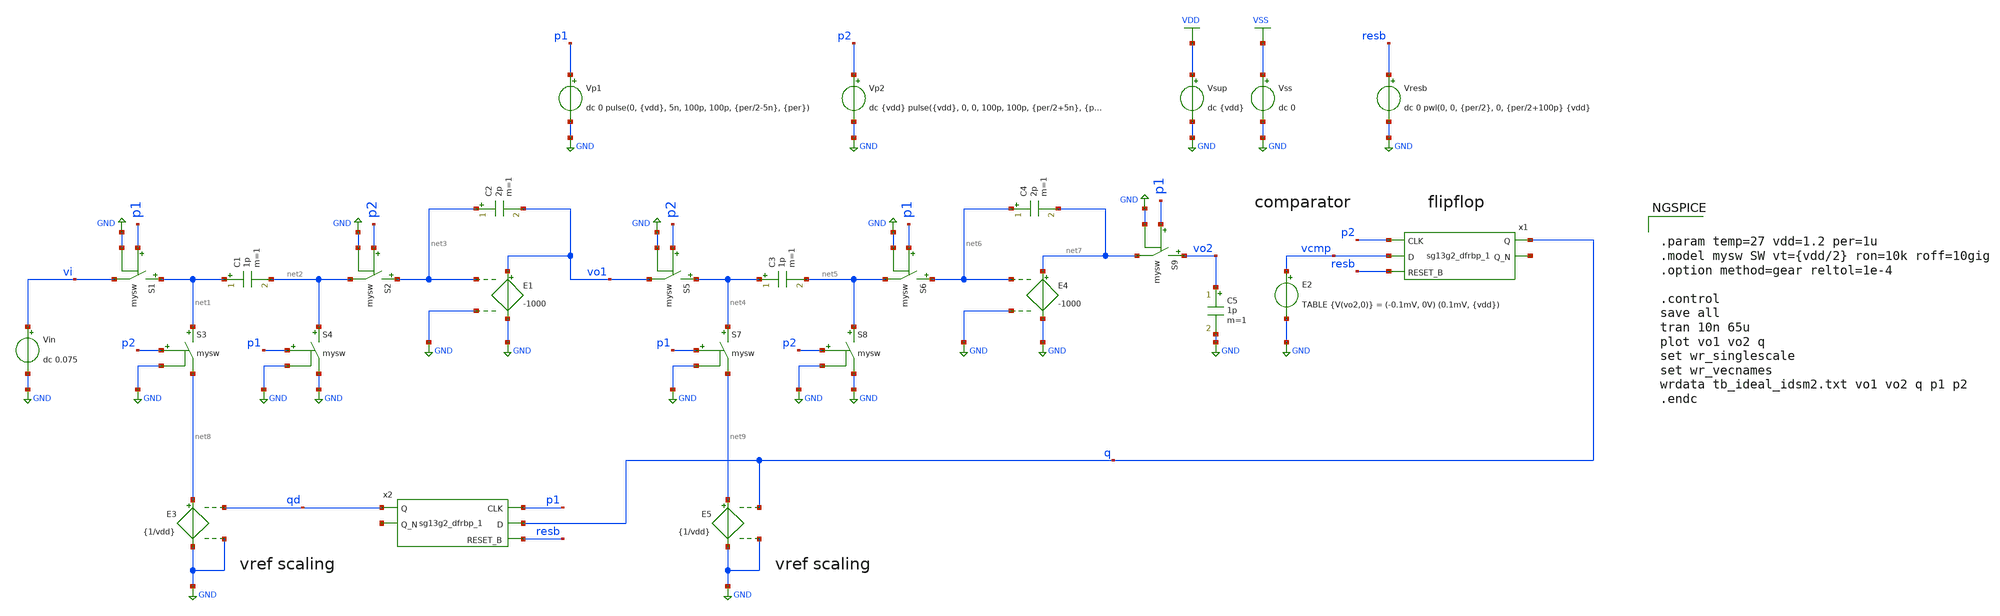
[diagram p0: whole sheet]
** sch_path: 5_Design/2_Idealized_circuits/tb_ideal_idsm2.sch
**.subckt tb_ideal_idsm2
Vp1 p1 GND dc 0 pulse(0, {vdd}, 5n, 100p, 100p, {per/2-5n}, {per})
E1 vo1 GND net3 GND -1000
S1 net1 vi p1 GND mysw
Vp2 p2 GND dc {vdd} pulse({vdd}, 0, 0, 100p, 100p, {per/2+5n}, {per})
Vin vi GND dc 0.075
C1 net1 net2 1p m=1
S2 net3 net2 p2 GND mysw
C2 net3 vo1 2p m=1
S3 net1 net8 p2 GND mysw
S4 net2 GND p1 GND mysw
E2 vcmp GND TABLE {V(vo2,0)} = (-0.1mV, 0V) (0.1mV, {vdd})
Vsup VDD GND dc {vdd}
E3 net8 GND qd GND {1/vdd}
Vresb resb GND dc 0 pwl(0, 0, {per/2}, 0, {per/2+100p} {vdd}
x1 q net10 p2 vcmp resb VDD VSS sg13g2_dfrbp_1
Vss VSS GND dc 0
E4 net7 GND net6 GND -1000
S5 net4 vo1 p2 GND mysw
C3 net4 net5 1p m=1
S6 net6 net5 p1 GND mysw
C4 net6 net7 2p m=1
S7 net4 net9 p1 GND mysw
S8 net5 GND p2 GND mysw
S9 vo2 net7 p1 GND mysw
C5 vo2 GND 1p m=1
E5 net9 GND q GND {1/vdd}
x2 qd net11 p1 q resb VDD VSS sg13g2_dfrbp_1
**** begin user architecture code

.lib $::SG13G2_MODELS/cornerMOSlv.lib mos_tt
.lib $::SG13G2_MODELS/cornerRES.lib res_typ
.inc /foss/pdks/sg13g2/libs.ref/sg13g2_stdcell/spice/sg13g2_stdcell.spice



.param temp=27 vdd=1.2 per=1u
.model mysw SW vt={vdd/2} ron=10k roff=10gig
.option method=gear reltol=1e-4

.control
save all
tran 10n 65u
plot vo1 vo2 q
set wr_singlescale
set wr_vecnames
wrdata tb_ideal_idsm2.txt vo1 vo2 q p1 p2
.endc


**** end user architecture code
**.ends

* expanding   symbol:  sg13g2_stdcells/sg13g2_dfrbp_1.sym # of pins=5
** sym_path: sg13g2_stdcells/sg13g2_dfrbp_1.sym
** sch_path: sg13g2_stdcells/sg13g2_dfrbp_1.sch
.subckt sg13g2_dfrbp_1 Q Q_N CLK D RESET_B VDD VSS
*.ipin D
*.ipin RESET_B
*.ipin CLK
*.opin Q
*.opin Q_N
*.iopin VDD
*.iopin VSS
XM1 Db D net10 VSS sg13_lv_nmos w=420.00n l=130.00n ng=1 m=1 mm_ok=1
XM2 net10 RESET_B VSS VSS sg13_lv_nmos w=420.00n l=130.00n ng=1 m=1 mm_ok=1
XM3 net1 clkneg net9 VSS sg13_lv_nmos w=420.00n l=130.00n ng=1 m=1 mm_ok=1
XM4 net9 net1 VSS VSS sg13_lv_nmos w=420.00n l=130.00n ng=1 m=1 mm_ok=1
XM5 net1 net1 net5 VSS sg13_lv_nmos w=420.00n l=130.00n ng=1 m=1 mm_ok=1
XM6 net5 RESET_B VSS VSS sg13_lv_nmos w=420.00n l=130.00n ng=1 m=1 mm_ok=1
XM7 Q_N net1 VSS VSS sg13_lv_nmos w=740.00n l=130.00n ng=1 m=1 mm_ok=1
XM8 net2 net1 VSS VSS sg13_lv_nmos w=740.00n l=130.00n ng=1 m=1 mm_ok=1
XM9 Q net2 VSS VSS sg13_lv_nmos w=740.00n l=130.00n ng=1 m=1 mm_ok=1
XM10 clkneg CLK VSS VSS sg13_lv_nmos w=740.00n l=130.00n ng=1 m=1 mm_ok=1
XM11 clkpos clkneg VSS VSS sg13_lv_nmos w=740.00n l=130.00n ng=1 m=1 mm_ok=1
XM12 Db clkneg net3 VSS sg13_lv_nmos w=420.00n l=130.00n ng=1 m=1 mm_ok=1
XM13 net3 clkpos net8 VSS sg13_lv_nmos w=420.00n l=130.00n ng=1 m=1 mm_ok=1
XM14 net8 net3 net4 VSS sg13_lv_nmos w=420.00n l=130.00n ng=1 m=1 mm_ok=1
XM15 net4 RESET_B VSS VSS sg13_lv_nmos w=420.00n l=130.00n ng=1 m=1 mm_ok=1
XM16 net3 net3 VSS VSS sg13_lv_nmos w=740.00n l=130.00n ng=1 m=1 mm_ok=1
XM17 net3 clkpos net1 VSS sg13_lv_nmos w=740.00n l=130.00n ng=1 m=1 mm_ok=1
XM18 Db RESET_B VDD VDD sg13_lv_pmos w=420.00n l=130.00n ng=1 m=1 mm_ok=1
XM19 Db D VDD VDD sg13_lv_pmos w=420.00n l=130.00n ng=1 m=1 mm_ok=1
XM20 net7 net1 VDD VDD sg13_lv_pmos w=420.00n l=130.00n ng=1 m=1 mm_ok=1
XM21 net1 clkpos net7 VDD sg13_lv_pmos w=420.00n l=130.00n ng=1 m=1 mm_ok=1
XM22 net1 net1 VDD VDD sg13_lv_pmos w=420.00n l=130.00n ng=1 m=1 mm_ok=1
XM23 net1 RESET_B VDD VDD sg13_lv_pmos w=420.00n l=130.00n ng=1 m=1 mm_ok=1
XM24 Q_N net1 VDD VDD sg13_lv_pmos w=1.12u l=130.00n ng=1 m=1 mm_ok=1
XM25 net2 net1 VDD VDD sg13_lv_pmos w=1.12u l=130.00n ng=1 m=1 mm_ok=1
XM26 Q net2 VDD VDD sg13_lv_pmos w=1.12u l=130.00n ng=1 m=1 mm_ok=1
XM27 clkneg CLK VDD VDD sg13_lv_pmos w=1.12u l=130.00n ng=1 m=1 mm_ok=1
XM28 clkpos clkneg VDD VDD sg13_lv_pmos w=1.12u l=130.00n ng=1 m=1 mm_ok=1
XM29 Db clkpos net3 VDD sg13_lv_pmos w=420.00n l=130.00n ng=1 m=1 mm_ok=1
XM30 net6 net3 VDD VDD sg13_lv_pmos w=420.00n l=130.00n ng=1 m=1 mm_ok=1
XM31 net3 clkneg net6 VDD sg13_lv_pmos w=420.00n l=130.00n ng=1 m=1 mm_ok=1
XM32 net3 RESET_B VDD VDD sg13_lv_pmos w=420.00n l=130.00n ng=1 m=1 mm_ok=1
XM33 net3 net3 VDD VDD sg13_lv_pmos w=1.000u l=130.00n ng=1 m=1 mm_ok=1
XM34 net3 clkneg net1 VDD sg13_lv_pmos w=1.000u l=130.00n ng=1 m=1 mm_ok=1
.ends

.GLOBAL GND
.GLOBAL VDD
.GLOBAL VSS
.end
